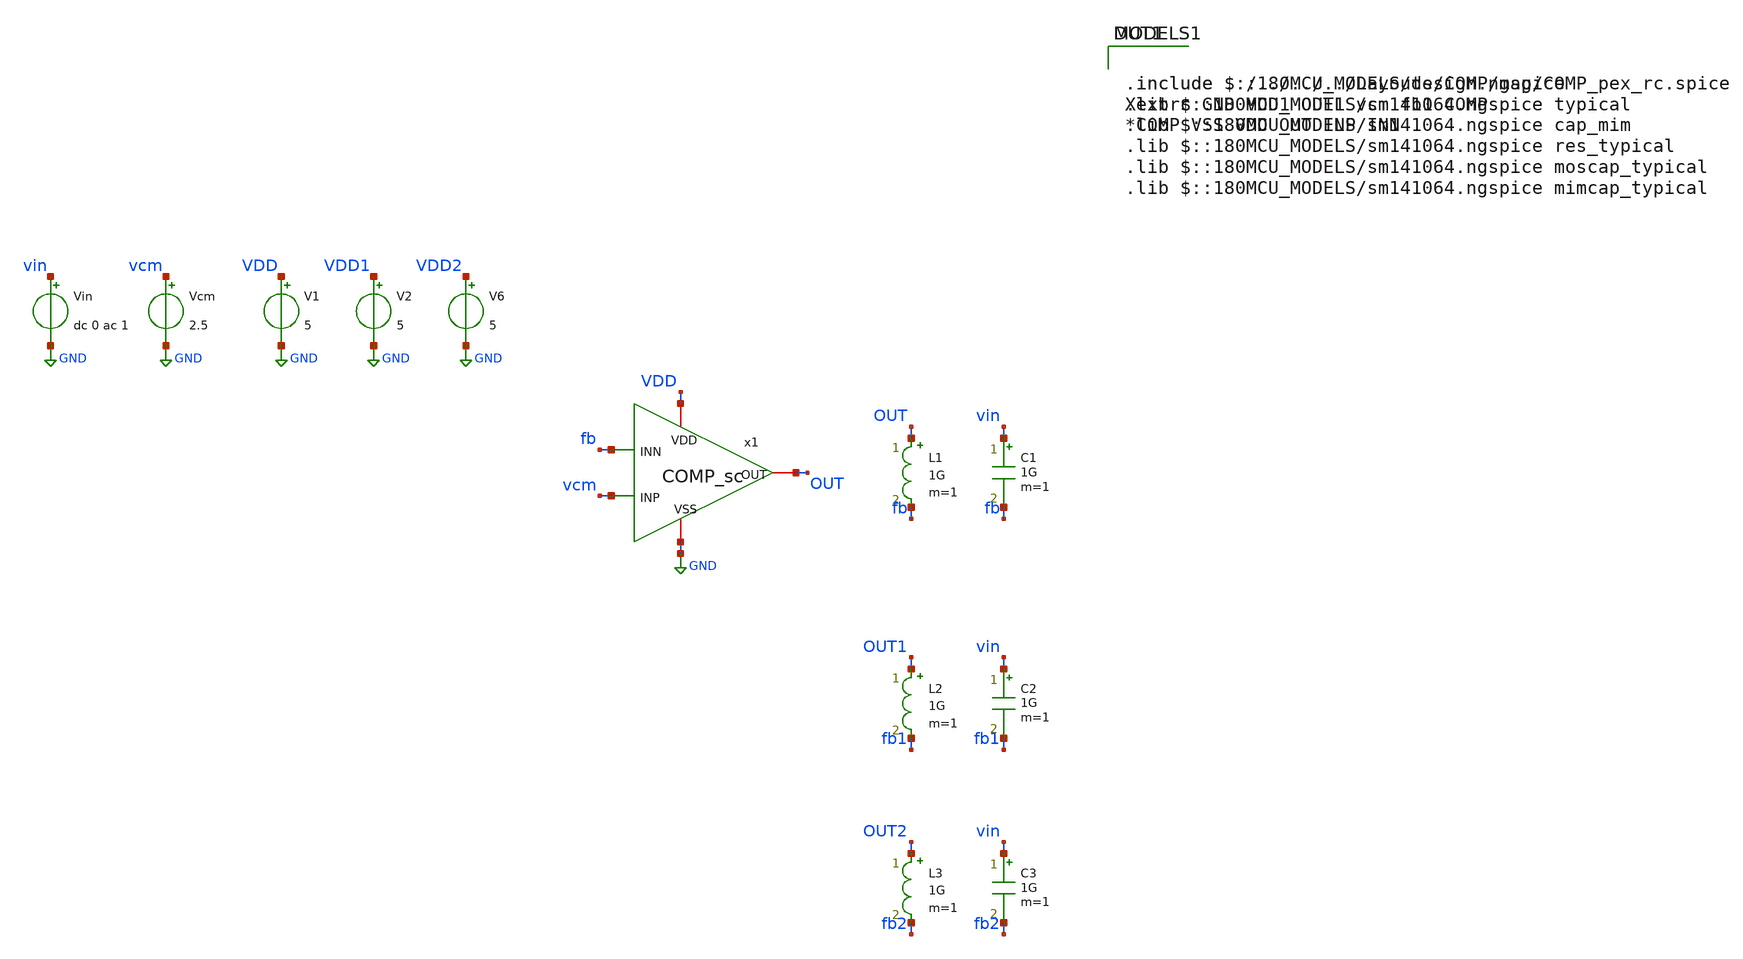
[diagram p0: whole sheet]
** sch_path: FINAL/XSCHEM/TEST/test_comp_ac.sch
**.subckt test_comp_ac
V1 VDD GND 5
V2 VDD1 GND 5
Vin vin GND dc 0 ac 1
Vcm vcm GND 2.5
x1 VDD fb OUT vcm GND COMP_sc
L1 OUT fb 1G m=1
C1 vin fb 1G m=1
L2 OUT1 fb1 1G m=1
C2 vin fb1 1G m=1
L3 OUT2 fb2 1G m=1
C3 vin fb2 1G m=1
V6 VDD2 GND 5
**** begin user architecture code

.include $::180MCU_MODELS/design.ngspice
.lib $::180MCU_MODELS/sm141064.ngspice typical
.lib $::180MCU_MODELS/sm141064.ngspice cap_mim
.lib $::180MCU_MODELS/sm141064.ngspice res_typical
.lib $::180MCU_MODELS/sm141064.ngspice moscap_typical
.lib $::180MCU_MODELS/sm141064.ngspice mimcap_typical


.include ../../../../Layouts/COMP/mag/COMP_pex_rc.spice
Xextrc GND VDD1 OUT1 vcm fb1 COMP
*COMP VSS VDD OUT INP INN


* La v2 del layout, con su propio lazo de autopolarizacion (L3/C3, nodo fb2) y
* su propia alimentacion, para poder medirla igual que a la v1.
.include ../../../../layouts_v2/COMP/mag/COMP_V2_pex_rc.spice
Xextrc2 GND VDD2 OUT2 vcm fb2 COMP_V2



* OJO: ni una llave en este texto. xschem las cuenta para saber donde acaba el
* bloque de atributos y una sola dentro de un comentario lo corta por la mitad,
* dejando el netlist con el 'blabla' de la plantilla y sin dar ningun error.
*
* No se puede atar la entrada en continua y lanzar un .ac: el punto de
* operacion cae saturado y linealizar ahi no significa nada. Cada rama lleva su
* lazo de L de 1 GH y C de 1 GF: en continua la L es un corto y el lazo unitario
* coloca al comparador en su propio offset; en alterna la L abre y la C
* cortocircuita, y lo que se mide es la ganancia en lazo abierto.
.save all
.control
ac dec 100 0.001 10G
wrdata ac.txt v(OUT) v(OUT1) v(OUT2)
.endc


**** end user architecture code
**.ends
.GLOBAL GND
.end
